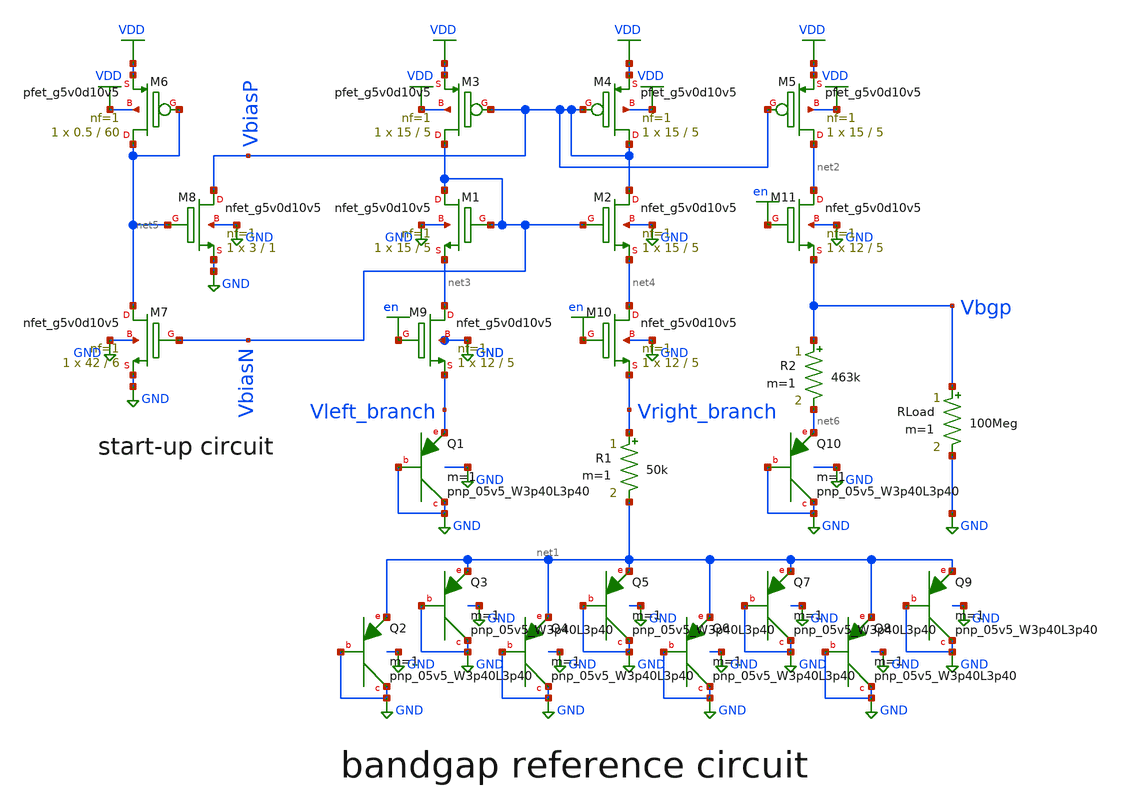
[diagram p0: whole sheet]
** sch_path: bandgap_sky130pdk.sch
**.subckt bandgap_sky130pdk
XM1 VbiasN VbiasN net3 GND sky130_fd_pr__nfet_g5v0d10v5 L=5 W=15 nf=1 ad='int((nf+1)/2) * W/nf * 0.29'
+ as='int((nf+2)/2) * W/nf * 0.29' pd='2*int((nf+1)/2) * (W/nf + 0.29)' ps='2*int((nf+2)/2) * (W/nf + 0.29)'
+ nrd='0.29 / W' nrs='0.29 / W' sa=0 sb=0 sd=0 mult=1 m=1
XM2 VbiasP VbiasN net4 GND sky130_fd_pr__nfet_g5v0d10v5 L=5 W=15 nf=1 ad='int((nf+1)/2) * W/nf * 0.29'
+ as='int((nf+2)/2) * W/nf * 0.29' pd='2*int((nf+1)/2) * (W/nf + 0.29)' ps='2*int((nf+2)/2) * (W/nf + 0.29)'
+ nrd='0.29 / W' nrs='0.29 / W' sa=0 sb=0 sd=0 mult=1 m=1
XM3 VbiasN VbiasP VDD VDD sky130_fd_pr__pfet_g5v0d10v5 L=5 W=15 nf=1 ad='int((nf+1)/2) * W/nf * 0.29'
+ as='int((nf+2)/2) * W/nf * 0.29' pd='2*int((nf+1)/2) * (W/nf + 0.29)' ps='2*int((nf+2)/2) * (W/nf + 0.29)'
+ nrd='0.29 / W' nrs='0.29 / W' sa=0 sb=0 sd=0 mult=1 m=1
XQ1 GND GND Vleft_branch sky130_fd_pr__pnp_05v5_W3p40L3p40 m=1
XQ2 GND GND net1 sky130_fd_pr__pnp_05v5_W3p40L3p40 m=1
XM5 net2 VbiasP VDD VDD sky130_fd_pr__pfet_g5v0d10v5 L=5 W=15 nf=1 ad='int((nf+1)/2) * W/nf * 0.29' as='int((nf+2)/2) * W/nf * 0.29'
+ pd='2*int((nf+1)/2) * (W/nf + 0.29)' ps='2*int((nf+2)/2) * (W/nf + 0.29)' nrd='0.29 / W' nrs='0.29 / W'
+ sa=0 sb=0 sd=0 mult=1 m=1
XQ3 GND GND net1 sky130_fd_pr__pnp_05v5_W3p40L3p40 m=1
XQ4 GND GND net1 sky130_fd_pr__pnp_05v5_W3p40L3p40 m=1
XQ5 GND GND net1 sky130_fd_pr__pnp_05v5_W3p40L3p40 m=1
XQ6 GND GND net1 sky130_fd_pr__pnp_05v5_W3p40L3p40 m=1
XQ7 GND GND net1 sky130_fd_pr__pnp_05v5_W3p40L3p40 m=1
XQ8 GND GND net1 sky130_fd_pr__pnp_05v5_W3p40L3p40 m=1
XQ9 GND GND net1 sky130_fd_pr__pnp_05v5_W3p40L3p40 m=1
R1 Vright_branch net1 50k m=1
R2 Vbgp net6 463k m=1
XQ10 GND GND net6 sky130_fd_pr__pnp_05v5_W3p40L3p40 m=1
XM4 VbiasP VbiasP VDD VDD sky130_fd_pr__pfet_g5v0d10v5 L=5 W=15 nf=1 ad='int((nf+1)/2) * W/nf * 0.29'
+ as='int((nf+2)/2) * W/nf * 0.29' pd='2*int((nf+1)/2) * (W/nf + 0.29)' ps='2*int((nf+2)/2) * (W/nf + 0.29)'
+ nrd='0.29 / W' nrs='0.29 / W' sa=0 sb=0 sd=0 mult=1 m=1
XM7 net5 VbiasN GND GND sky130_fd_pr__nfet_g5v0d10v5 L=6 W=42 nf=1 ad='int((nf+1)/2) * W/nf * 0.29' as='int((nf+2)/2) * W/nf * 0.29'
+ pd='2*int((nf+1)/2) * (W/nf + 0.29)' ps='2*int((nf+2)/2) * (W/nf + 0.29)' nrd='0.29 / W' nrs='0.29 / W'
+ sa=0 sb=0 sd=0 mult=1 m=1
XM8 VbiasP net5 GND GND sky130_fd_pr__nfet_g5v0d10v5 L=1 W=3 nf=1 ad='int((nf+1)/2) * W/nf * 0.29' as='int((nf+2)/2) * W/nf * 0.29'
+ pd='2*int((nf+1)/2) * (W/nf + 0.29)' ps='2*int((nf+2)/2) * (W/nf + 0.29)' nrd='0.29 / W' nrs='0.29 / W'
+ sa=0 sb=0 sd=0 mult=1 m=1
RLoad Vbgp GND 100Meg m=1
XM9 net3 en Vleft_branch GND sky130_fd_pr__nfet_g5v0d10v5 L=5 W=12 nf=1 ad='int((nf+1)/2) * W/nf * 0.29'
+ as='int((nf+2)/2) * W/nf * 0.29' pd='2*int((nf+1)/2) * (W/nf + 0.29)' ps='2*int((nf+2)/2) * (W/nf + 0.29)'
+ nrd='0.29 / W' nrs='0.29 / W' sa=0 sb=0 sd=0 mult=1 m=1
XM10 net4 en Vright_branch GND sky130_fd_pr__nfet_g5v0d10v5 L=5 W=12 nf=1 ad='int((nf+1)/2) * W/nf * 0.29'
+ as='int((nf+2)/2) * W/nf * 0.29' pd='2*int((nf+1)/2) * (W/nf + 0.29)' ps='2*int((nf+2)/2) * (W/nf + 0.29)'
+ nrd='0.29 / W' nrs='0.29 / W' sa=0 sb=0 sd=0 mult=1 m=1
XM11 net2 en Vbgp GND sky130_fd_pr__nfet_g5v0d10v5 L=5 W=12 nf=1 ad='int((nf+1)/2) * W/nf * 0.29' as='int((nf+2)/2) * W/nf * 0.29'
+ pd='2*int((nf+1)/2) * (W/nf + 0.29)' ps='2*int((nf+2)/2) * (W/nf + 0.29)' nrd='0.29 / W' nrs='0.29 / W'
+ sa=0 sb=0 sd=0 mult=1 m=1
XM6 net5 net5 VDD VDD sky130_fd_pr__pfet_g5v0d10v5 L=60 W=0.5 nf=1 ad='int((nf+1)/2) * W/nf * 0.29' as='int((nf+2)/2) * W/nf * 0.29'
+ pd='2*int((nf+1)/2) * (W/nf + 0.29)' ps='2*int((nf+2)/2) * (W/nf + 0.29)' nrd='0.29 / W' nrs='0.29 / W'
+ sa=0 sb=0 sd=0 mult=1 m=1
**** begin user architecture code


.lib /usr/local/share/pdk/sky130A/libs.tech/ngspice/sky130.lib.spice tt
.options savecurrents
*** plot vbgp with variation in supply voltage
*Vdd VDD GND 3.3
*V_en en GND 3.3
*.dc Vdd 2 4 0.1
*.control
*run
*print Vbgp
*plot V(Vbgp)
*.endc
*** plot vbgp with variation in temperature @3.3V
*Vdd VDD GND 3.3
*V_en en GND 3.3
*.dc temp -40 140 1
*.control
*run
*print V(Vbgp)
*plot V(Vbgp)
*.endc
*** plot voltage coefficient
*Vdd VDD GND 3.3
*V_en en GND 3.3
*.dc Vdd 2 4 0.1
*.control
*run
*plot deriv(V(Vbgp))
*.endc
*** plot temperature coefficient
*Vdd VDD GND 3.3
*V_en en GND 3.3
*.dc temp -40 140 1
*.control
*run
*plot deriv(V(Vbgp))/1.202344
*.endc
*** check start up circuit
V_en en GND 3.3
Vdd VDD GND PULSE(0 3.3 50us 200us 200us 600us 2000us 0)
.tran 1us 800us
.control
run
plot V(Vdd) V(Vbgp)
.endc
*** enable pin
*Vdd VDD GND 3.3
*V_en en GND PULSE(0 3.3 0 200us 200us 600us 2000us 0)
*.tran 1u 2000us
*.control
*run
*plot V(en)
*plot -I(VDD)
*.endc


**** end user architecture code
**.ends
.GLOBAL GND
.GLOBAL VDD
.GLOBAL en
.end
